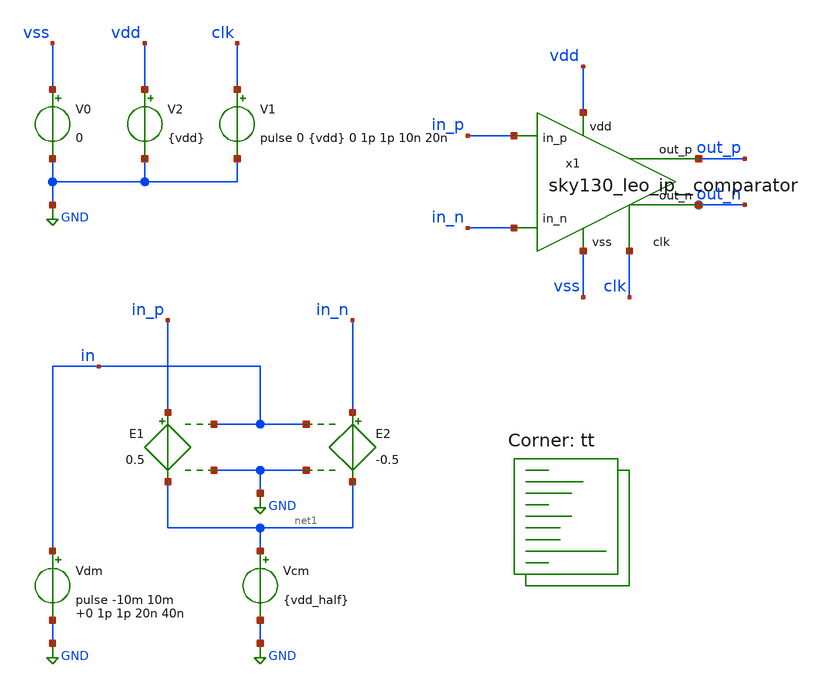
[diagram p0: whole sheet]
** sch_path: custom_gds/tt_um_tt08_aicd_playground/dependencies/sky130_leo_ip__comparator/xschem/sky130_leo_ip__comparator_tb.sch

.include $PDK_ROOT/$PDK/libs.ref/sky130_fd_sc_hvl/spice/sky130_fd_sc_hvl.spice

**.subckt sky130_leo_ip__comparator_tb
E1 in_p net1 in GND 0.5
E2 in_n net1 in GND -0.5
Vcm net1 GND {vdd_half}
V0 vss GND 0
V2 vdd GND {vdd}
V1 clk GND pulse 0 {vdd} 0 1p 1p 10n 20n
Vdm in GND pulse -10m 10m 0 1p 1p 20n 40n
x1 vdd in_p out_p in_n vss clk out_n sky130_leo_ip__comparator
**** begin user architecture code
.lib $::SKYWATER_MODELS/sky130.lib.spice tt



.param vdd = 3.3
.param vdd_half = 1.65

*.include {DUT_path}

.control
    save all

    * save id, gm, gds
    save @m.x1.xm5.msky130_fd_pr__nfet_g5v0d10v5[id] @m.x1.xm5.msky130_fd_pr__nfet_g5v0d10v5[gm]
+ @m.x1.xm5.msky130_fd_pr__nfet_g5v0d10v5[gds]
    save @m.x1.xm6.msky130_fd_pr__nfet_g5v0d10v5[id] @m.x1.xm6.msky130_fd_pr__nfet_g5v0d10v5[gm]
+ @m.x1.xm6.msky130_fd_pr__nfet_g5v0d10v5[gds]
    save @m.x1.xm7.msky130_fd_pr__nfet_g5v0d10v5[id] @m.x1.xm7.msky130_fd_pr__nfet_g5v0d10v5[gm]
+ @m.x1.xm7.msky130_fd_pr__nfet_g5v0d10v5[gds]

    save @m.x1.xm1.msky130_fd_pr__pfet_g5v0d10v5[id] @m.x1.xm1.msky130_fd_pr__pfet_g5v0d10v5[gm]
+ @m.x1.xm1.msky130_fd_pr__pfet_g5v0d10v5[gds]
    save @m.x1.xm2.msky130_fd_pr__pfet_g5v0d10v5[id] @m.x1.xm2.msky130_fd_pr__pfet_g5v0d10v5[gm]
+ @m.x1.xm2.msky130_fd_pr__pfet_g5v0d10v5[gds]
    save @m.x1.xm3.msky130_fd_pr__pfet_g5v0d10v5[id] @m.x1.xm3.msky130_fd_pr__pfet_g5v0d10v5[gm]
+ @m.x1.xm4.msky130_fd_pr__pfet_g5v0d10v5[gds]
    save @m.x1.xm4.msky130_fd_pr__pfet_g5v0d10v5[id] @m.x1.xm4.msky130_fd_pr__pfet_g5v0d10v5[gm]
+ @m.x1.xm5.msky130_fd_pr__pfet_g5v0d10v5[gds]

    * operating point
    op
    write sky130_leo_ip_comparator_tb.raw
    set appendwrite

    * transient simulation
    options method=gear
    tran 10p 80n
    save all
    write sky130_leo_ip_comparator_tb.raw


    * measure paramters
    *let vout_mag = abs(v(out))
    *let vout_phase_margin = phase(v(out)) * 180/pi + 180
    let out = v(out_p) - v(out_n)
    meas tran pval find out AT=19.9n
    meas tran nval find out AT=39.9n
    *meas ac A0 find vout_mag at=1k
    *meas ac UGF when vout_mag=1 fall=1
    *meas ac PM find vout_phase_margin when vout_mag=1

    *echo $&ugf > {simpath}/{filename}_{N}.data
    *quit

    * The threshold of +/- 1.0V is quite arbitrary
    if pval > 1.0 and nval < -1.0
        echo Ok!
    else
        echo Not Ok!
    end
.endc



**** end user architecture code
**.ends

* expanding   symbol:  sky130_leo_ip__comparator.sym # of pins=7
** sym_path: custom_gds/tt_um_tt08_aicd_playground/dependencies/sky130_leo_ip__comparator/xschem/sky130_leo_ip__comparator.sym
** sch_path: custom_gds/tt_um_tt08_aicd_playground/dependencies/sky130_leo_ip__comparator/xschem/sky130_leo_ip__comparator.sch
.subckt sky130_leo_ip__comparator vdd in_p out_p in_n vss clk out_n
*.opin out_n
*.ipin in_p
*.ipin in_n
*.iopin vdd
*.iopin vss
*.ipin clk
*.opin out_p
XR1 vss net2 vss sky130_fd_pr__res_xhigh_po_2p85 L=25 mult=1 m=1
XM7 comp_p comp_n vss vss sky130_fd_pr__nfet_g5v0d10v5 L=0.5 W=5 nf=1 ad='int((nf+1)/2) * W/nf * 0.29'
+ as='int((nf+2)/2) * W/nf * 0.29' pd='2*int((nf+1)/2) * (W/nf + 0.29)' ps='2*int((nf+2)/2) * (W/nf + 0.29)'
+ nrd='0.29 / W' nrs='0.29 / W' sa=0 sb=0 sd=0 mult=1 m=1
XM1 net2 net2 vdd vdd sky130_fd_pr__pfet_g5v0d10v5 L=5 W=1 nf=1 ad='int((nf+1)/2) * W/nf * 0.29' as='int((nf+2)/2) * W/nf * 0.29'
+ pd='2*int((nf+1)/2) * (W/nf + 0.29)' ps='2*int((nf+2)/2) * (W/nf + 0.29)' nrd='0.29 / W' nrs='0.29 / W'
+ sa=0 sb=0 sd=0 mult=1 m=1
XM6 comp_n comp_p vss vss sky130_fd_pr__nfet_g5v0d10v5 L=0.5 W=5 nf=1 ad='int((nf+1)/2) * W/nf * 0.29'
+ as='int((nf+2)/2) * W/nf * 0.29' pd='2*int((nf+1)/2) * (W/nf + 0.29)' ps='2*int((nf+2)/2) * (W/nf + 0.29)'
+ nrd='0.29 / W' nrs='0.29 / W' sa=0 sb=0 sd=0 mult=1 m=1
XM2 net1 net2 vdd vdd sky130_fd_pr__pfet_g5v0d10v5 L=5 W=10 nf=1 ad='int((nf+1)/2) * W/nf * 0.29' as='int((nf+2)/2) * W/nf * 0.29'
+ pd='2*int((nf+1)/2) * (W/nf + 0.29)' ps='2*int((nf+2)/2) * (W/nf + 0.29)' nrd='0.29 / W' nrs='0.29 / W'
+ sa=0 sb=0 sd=0 mult=1 m=1
XM4 comp_p in_n net1 vdd sky130_fd_pr__pfet_g5v0d10v5 L=0.5 W=20 nf=1 ad='int((nf+1)/2) * W/nf * 0.29'
+ as='int((nf+2)/2) * W/nf * 0.29' pd='2*int((nf+1)/2) * (W/nf + 0.29)' ps='2*int((nf+2)/2) * (W/nf + 0.29)'
+ nrd='0.29 / W' nrs='0.29 / W' sa=0 sb=0 sd=0 mult=1 m=1
XM3 comp_n in_p net1 vdd sky130_fd_pr__pfet_g5v0d10v5 L=0.5 W=20 nf=1 ad='int((nf+1)/2) * W/nf * 0.29'
+ as='int((nf+2)/2) * W/nf * 0.29' pd='2*int((nf+1)/2) * (W/nf + 0.29)' ps='2*int((nf+2)/2) * (W/nf + 0.29)'
+ nrd='0.29 / W' nrs='0.29 / W' sa=0 sb=0 sd=0 mult=1 m=1
XM5 comp_n clk comp_p vss sky130_fd_pr__nfet_g5v0d10v5 L=0.5 W=10 nf=1 ad='int((nf+1)/2) * W/nf * 0.29'
+ as='int((nf+2)/2) * W/nf * 0.29' pd='2*int((nf+1)/2) * (W/nf + 0.29)' ps='2*int((nf+2)/2) * (W/nf + 0.29)'
+ nrd='0.29 / W' nrs='0.29 / W' sa=0 sb=0 sd=0 mult=1 m=1
x1 SR_set_n net4 VSS VSS VDD VDD net3 sky130_fd_sc_hvl__nand2_1
x2 net3 SR_reset_n VSS VSS VDD VDD net4 sky130_fd_sc_hvl__nand2_1
XM8 SR_set_n comp_p vdd vdd sky130_fd_pr__pfet_g5v0d10v5 L=0.5 W=5 nf=1 ad='int((nf+1)/2) * W/nf * 0.29'
+ as='int((nf+2)/2) * W/nf * 0.29' pd='2*int((nf+1)/2) * (W/nf + 0.29)' ps='2*int((nf+2)/2) * (W/nf + 0.29)'
+ nrd='0.29 / W' nrs='0.29 / W' sa=0 sb=0 sd=0 mult=1 m=1
XM9 SR_set_n comp_p vss vss sky130_fd_pr__nfet_g5v0d10v5 L=0.5 W=1 nf=1 ad='int((nf+1)/2) * W/nf * 0.29'
+ as='int((nf+2)/2) * W/nf * 0.29' pd='2*int((nf+1)/2) * (W/nf + 0.29)' ps='2*int((nf+2)/2) * (W/nf + 0.29)'
+ nrd='0.29 / W' nrs='0.29 / W' sa=0 sb=0 sd=0 mult=1 m=1
XM10 SR_reset_n comp_n vdd vdd sky130_fd_pr__pfet_g5v0d10v5 L=0.5 W=5 nf=1 ad='int((nf+1)/2) * W/nf * 0.29'
+ as='int((nf+2)/2) * W/nf * 0.29' pd='2*int((nf+1)/2) * (W/nf + 0.29)' ps='2*int((nf+2)/2) * (W/nf + 0.29)'
+ nrd='0.29 / W' nrs='0.29 / W' sa=0 sb=0 sd=0 mult=1 m=1
XM11 SR_reset_n comp_n vss vss sky130_fd_pr__nfet_g5v0d10v5 L=0.5 W=1 nf=1 ad='int((nf+1)/2) * W/nf * 0.29'
+ as='int((nf+2)/2) * W/nf * 0.29' pd='2*int((nf+1)/2) * (W/nf + 0.29)' ps='2*int((nf+2)/2) * (W/nf + 0.29)'
+ nrd='0.29 / W' nrs='0.29 / W' sa=0 sb=0 sd=0 mult=1 m=1
x3 net3 VSS VSS VDD VDD out_p sky130_fd_sc_hvl__buf_4
x4 net4 VSS VSS VDD VDD out_n sky130_fd_sc_hvl__buf_4
.ends

.GLOBAL GND
.end
